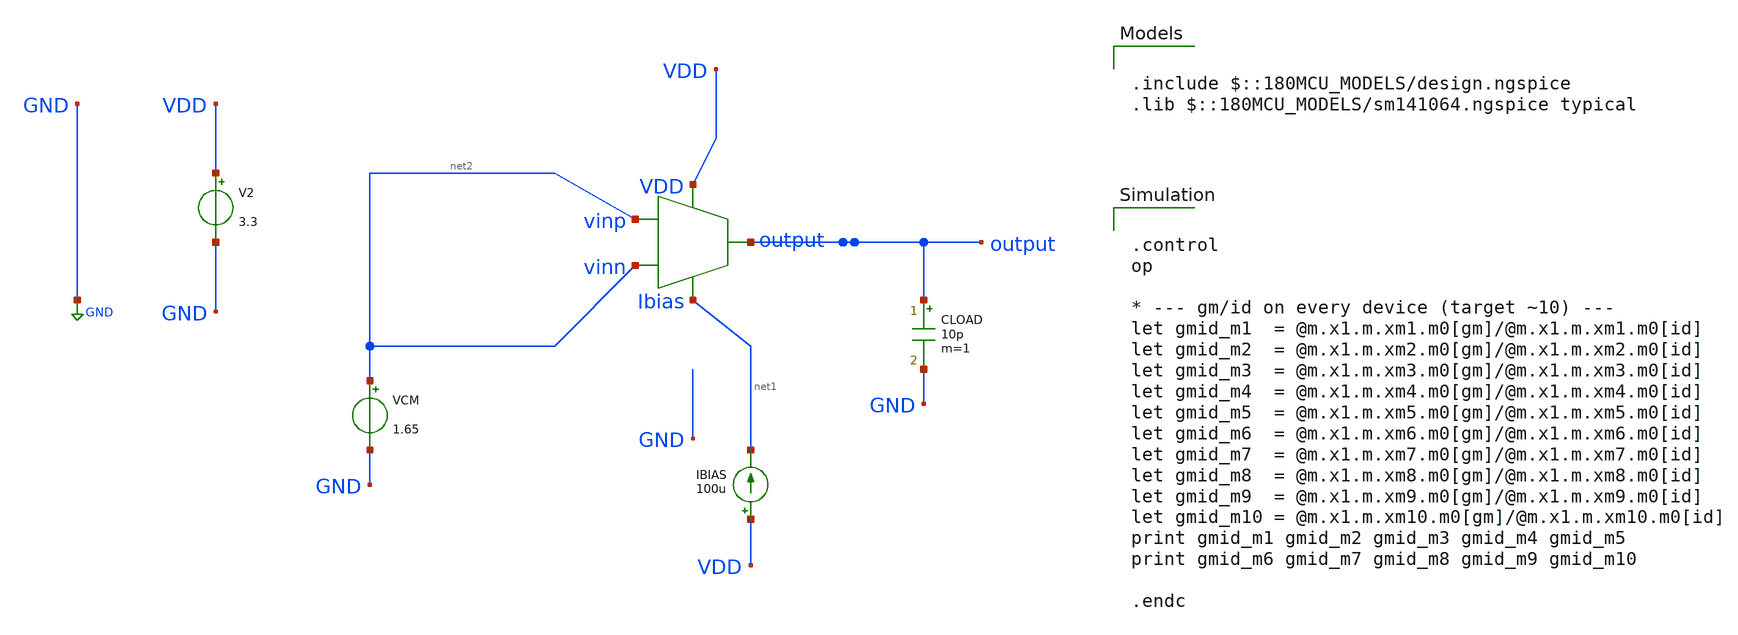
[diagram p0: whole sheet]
** sch_path: designs/libs/core_amps/ota_telescopic/tb/telescopic_op_gmid_tb.sch
**.subckt telescopic_op_gmid_tb
IBIAS VDD net1 100u
V2 VDD GND 3.3
CLOAD output GND 10p m=1
VCM net2 GND 1.65
X1 net2 net2 VDD net1 output telescopic_cascode
**** begin user architecture code

.include $::180MCU_MODELS/design.ngspice
.lib $::180MCU_MODELS/sm141064.ngspice typical



.control
op

* --- gm/id on every device (target ~10) ---
let gmid_m1  = @m.x1.m.xm1.m0[gm]/@m.x1.m.xm1.m0[id]
let gmid_m2  = @m.x1.m.xm2.m0[gm]/@m.x1.m.xm2.m0[id]
let gmid_m3  = @m.x1.m.xm3.m0[gm]/@m.x1.m.xm3.m0[id]
let gmid_m4  = @m.x1.m.xm4.m0[gm]/@m.x1.m.xm4.m0[id]
let gmid_m5  = @m.x1.m.xm5.m0[gm]/@m.x1.m.xm5.m0[id]
let gmid_m6  = @m.x1.m.xm6.m0[gm]/@m.x1.m.xm6.m0[id]
let gmid_m7  = @m.x1.m.xm7.m0[gm]/@m.x1.m.xm7.m0[id]
let gmid_m8  = @m.x1.m.xm8.m0[gm]/@m.x1.m.xm8.m0[id]
let gmid_m9  = @m.x1.m.xm9.m0[gm]/@m.x1.m.xm9.m0[id]
let gmid_m10 = @m.x1.m.xm10.m0[gm]/@m.x1.m.xm10.m0[id]
print gmid_m1 gmid_m2 gmid_m3 gmid_m4 gmid_m5
print gmid_m6 gmid_m7 gmid_m8 gmid_m9 gmid_m10

.endc


**** end user architecture code
**.ends

* expanding   symbol:  libs/core_amps/ota_telescopic/telescopic_cascode.sym # of pins=5
** sym_path: designs/libs/core_amps/ota_telescopic/telescopic_cascode.sym
** sch_path: designs/libs/core_amps/ota_telescopic/telescopic_cascode.sch
.subckt telescopic_cascode vinp vinn VDD Ibias output
*.ipin vinp
*.ipin vinn
*.opin output
*.iopin Ibias
*.iopin VDD
XM8 output net4 net3 VDD pfet_03v3 L=0.56u W=65u nf=1 ad='int((nf+1)/2) * W/nf * 0.18u' as='int((nf+2)/2) * W/nf * 0.18u'
+ pd='2*int((nf+1)/2) * (W/nf + 0.18u)' ps='2*int((nf+2)/2) * (W/nf + 0.18u)' nrd='0.18u / W' nrs='0.18u / W'
+ sa=0 sb=0 sd=0 m=4
XM4 output VBN1 net7 GND nfet_03v3 L=0.5u W=40u nf=1 ad='int((nf+1)/2) * W/nf * 0.18u' as='int((nf+2)/2) * W/nf * 0.18u'
+ pd='2*int((nf+1)/2) * (W/nf + 0.18u)' ps='2*int((nf+2)/2) * (W/nf + 0.18u)' nrd='0.18u / W' nrs='0.18u / W'
+ sa=0 sb=0 sd=0 m=1
XM1 net5 vinp net6 GND nfet_03v3 L=0.5u W=30u nf=1 ad='int((nf+1)/2) * W/nf * 0.18u' as='int((nf+2)/2) * W/nf * 0.18u'
+ pd='2*int((nf+1)/2) * (W/nf + 0.18u)' ps='2*int((nf+2)/2) * (W/nf + 0.18u)' nrd='0.18u / W' nrs='0.18u / W'
+ sa=0 sb=0 sd=0 m=1
XM2 net1 VBN1 net5 GND nfet_03v3 L=0.5u W=40u nf=1 ad='int((nf+1)/2) * W/nf * 0.18u' as='int((nf+2)/2) * W/nf * 0.18u'
+ pd='2*int((nf+1)/2) * (W/nf + 0.18u)' ps='2*int((nf+2)/2) * (W/nf + 0.18u)' nrd='0.18u / W' nrs='0.18u / W'
+ sa=0 sb=0 sd=0 m=1
XM3 net7 vinn net6 GND nfet_03v3 L=0.5u W=30u nf=1 ad='int((nf+1)/2) * W/nf * 0.18u' as='int((nf+2)/2) * W/nf * 0.18u'
+ pd='2*int((nf+1)/2) * (W/nf + 0.18u)' ps='2*int((nf+2)/2) * (W/nf + 0.18u)' nrd='0.18u / W' nrs='0.18u / W'
+ sa=0 sb=0 sd=0 m=1
XM5 net3 net1 VDD VDD pfet_03v3 L=0.56u W=65u nf=1 ad='int((nf+1)/2) * W/nf * 0.18u' as='int((nf+2)/2) * W/nf * 0.18u'
+ pd='2*int((nf+1)/2) * (W/nf + 0.18u)' ps='2*int((nf+2)/2) * (W/nf + 0.18u)' nrd='0.18u / W' nrs='0.18u / W'
+ sa=0 sb=0 sd=0 m=4
XM6 net1 net4 net2 VDD pfet_03v3 L=0.56u W=65u nf=1 ad='int((nf+1)/2) * W/nf * 0.18u' as='int((nf+2)/2) * W/nf * 0.18u'
+ pd='2*int((nf+1)/2) * (W/nf + 0.18u)' ps='2*int((nf+2)/2) * (W/nf + 0.18u)' nrd='0.18u / W' nrs='0.18u / W'
+ sa=0 sb=0 sd=0 m=4
XM7 net2 net1 VDD VDD pfet_03v3 L=0.56u W=65u nf=1 ad='int((nf+1)/2) * W/nf * 0.18u' as='int((nf+2)/2) * W/nf * 0.18u'
+ pd='2*int((nf+1)/2) * (W/nf + 0.18u)' ps='2*int((nf+2)/2) * (W/nf + 0.18u)' nrd='0.18u / W' nrs='0.18u / W'
+ sa=0 sb=0 sd=0 m=4
XM9 net6 Ibias GND GND nfet_03v3 L=0.28u W=15.54u nf=1 ad='int((nf+1)/2) * W/nf * 0.18u' as='int((nf+2)/2) * W/nf * 0.18u'
+ pd='2*int((nf+1)/2) * (W/nf + 0.18u)' ps='2*int((nf+2)/2) * (W/nf + 0.18u)' nrd='0.18u / W' nrs='0.18u / W'
+ sa=0 sb=0 sd=0 m=1
XM10 Ibias Ibias GND GND nfet_03v3 L=.28u W=5.18u nf=1 ad='int((nf+1)/2) * W/nf * 0.18u' as='int((nf+2)/2) * W/nf * 0.18u'
+ pd='2*int((nf+1)/2) * (W/nf + 0.18u)' ps='2*int((nf+2)/2) * (W/nf + 0.18u)' nrd='0.18u / W' nrs='0.18u / W'
+ sa=0 sb=0 sd=0 m=1
**** begin user architecture code


.include /foss/pdks/gf180mcuD/libs.tech/ngspice/design.ngspice
.lib /foss/pdks/gf180mcuD/libs.tech/ngspice/sm141064.ngspice typical

**** end user architecture code
V1 VBN1 GND 2.2
V2 net4 GND 1.6
.ends

.GLOBAL GND
.end
